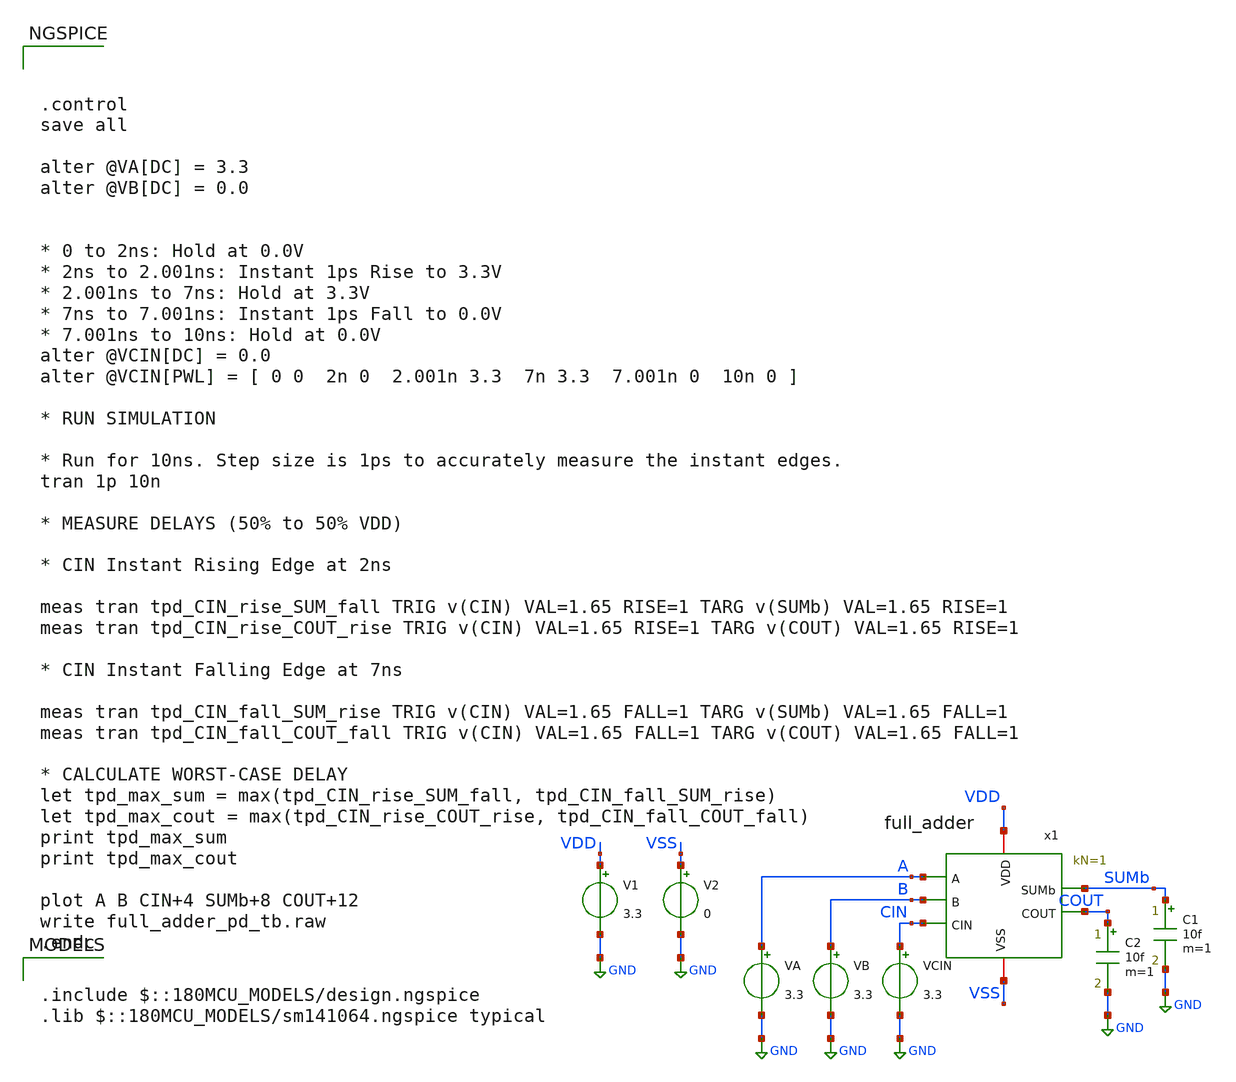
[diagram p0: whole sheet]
** sch_path: CAD4/full_adder_pd_tb.sch
**.subckt full_adder_pd_tb
V1 VDD GND 3.3
VA A GND 3.3
VB B GND 3.3
VCIN CIN GND 3.3
C1 SUMb GND 10f m=1
V2 VSS GND 0
x1 VDD VSS A B CIN SUMb COUT full_adder kN=1 kM=1
C2 COUT GND 10f m=1
**** begin user architecture code

.include $::180MCU_MODELS/design.ngspice
.lib $::180MCU_MODELS/sm141064.ngspice typical




.control
save all

alter @VA[DC] = 3.3
alter @VB[DC] = 0.0


* 0 to 2ns: Hold at 0.0V
* 2ns to 2.001ns: Instant 1ps Rise to 3.3V
* 2.001ns to 7ns: Hold at 3.3V
* 7ns to 7.001ns: Instant 1ps Fall to 0.0V
* 7.001ns to 10ns: Hold at 0.0V
alter @VCIN[DC] = 0.0
alter @VCIN[PWL] = [ 0 0  2n 0  2.001n 3.3  7n 3.3  7.001n 0  10n 0 ]

* RUN SIMULATION

* Run for 10ns. Step size is 1ps to accurately measure the instant edges.
tran 1p 10n

* MEASURE DELAYS (50% to 50% VDD)

* CIN Instant Rising Edge at 2ns

meas tran tpd_CIN_rise_SUM_fall TRIG v(CIN) VAL=1.65 RISE=1 TARG v(SUMb) VAL=1.65 RISE=1
meas tran tpd_CIN_rise_COUT_rise TRIG v(CIN) VAL=1.65 RISE=1 TARG v(COUT) VAL=1.65 RISE=1

* CIN Instant Falling Edge at 7ns

meas tran tpd_CIN_fall_SUM_rise TRIG v(CIN) VAL=1.65 FALL=1 TARG v(SUMb) VAL=1.65 FALL=1
meas tran tpd_CIN_fall_COUT_fall TRIG v(CIN) VAL=1.65 FALL=1 TARG v(COUT) VAL=1.65 FALL=1

* CALCULATE WORST-CASE DELAY
let tpd_max_sum = max(tpd_CIN_rise_SUM_fall, tpd_CIN_fall_SUM_rise)
let tpd_max_cout = max(tpd_CIN_rise_COUT_rise, tpd_CIN_fall_COUT_fall)
print tpd_max_sum
print tpd_max_cout

plot A B CIN+4 SUMb+8 COUT+12
write full_adder_pd_tb.raw
.endc


**** end user architecture code
**.ends

* expanding   symbol:  engn1600-team1/CAD4/full_adder.sym # of pins=7
** sym_path: CAD4/full_adder.sym
** sch_path: CAD4/full_adder.sch
.subckt full_adder VDD VSS A B CIN SUMb COUT  kN=1 kM=1
*.iopin VDD
*.iopin VSS
*.ipin A
*.ipin B
*.ipin CIN
*.opin SUMb
*.opin COUT
XM1 net1 B VDD VDD pfet_03v3 L=0.28u W=0.72u nf=1 ad='int((nf+1)/2) * W/nf * 0.18u' as='int((nf+2)/2) * W/nf * 0.18u'
+ pd='2*int((nf+1)/2) * (W/nf + 0.18u)' ps='2*int((nf+2)/2) * (W/nf + 0.18u)' nrd='0.18u / W' nrs='0.18u / W'
+ sa=0 sb=0 sd=0 m=1
XM2 net4 A net1 VDD pfet_03v3 L=0.28u W=0.72u nf=1 ad='int((nf+1)/2) * W/nf * 0.18u' as='int((nf+2)/2) * W/nf * 0.18u'
+ pd='2*int((nf+1)/2) * (W/nf + 0.18u)' ps='2*int((nf+2)/2) * (W/nf + 0.18u)' nrd='0.18u / W' nrs='0.18u / W'
+ sa=0 sb=0 sd=0 m=1
XM3 net3 A VDD VDD pfet_03v3 L=0.28u W=0.72u nf=1 ad='int((nf+1)/2) * W/nf * 0.18u' as='int((nf+2)/2) * W/nf * 0.18u'
+ pd='2*int((nf+1)/2) * (W/nf + 0.18u)' ps='2*int((nf+2)/2) * (W/nf + 0.18u)' nrd='0.18u / W' nrs='0.18u / W'
+ sa=0 sb=0 sd=0 m=1
XM4 net3 B VDD VDD pfet_03v3 L=0.28u W=0.72u nf=1 ad='int((nf+1)/2) * W/nf * 0.18u' as='int((nf+2)/2) * W/nf * 0.18u'
+ pd='2*int((nf+1)/2) * (W/nf + 0.18u)' ps='2*int((nf+2)/2) * (W/nf + 0.18u)' nrd='0.18u / W' nrs='0.18u / W'
+ sa=0 sb=0 sd=0 m=1
XM5 net4 CIN net3 VDD pfet_03v3 L=0.28u W=0.72u nf=1 ad='int((nf+1)/2) * W/nf * 0.18u' as='int((nf+2)/2) * W/nf * 0.18u'
+ pd='2*int((nf+1)/2) * (W/nf + 0.18u)' ps='2*int((nf+2)/2) * (W/nf + 0.18u)' nrd='0.18u / W' nrs='0.18u / W'
+ sa=0 sb=0 sd=0 m=1
XM6 net4 CIN net5 VSS nfet_03v3 L=0.28u W=0.36u nf=1 ad='int((nf+1)/2) * W/nf * 0.18u' as='int((nf+2)/2) * W/nf * 0.18u'
+ pd='2*int((nf+1)/2) * (W/nf + 0.18u)' ps='2*int((nf+2)/2) * (W/nf + 0.18u)' nrd='0.18u / W' nrs='0.18u / W'
+ sa=0 sb=0 sd=0 m=1
XM7 net2 B VSS VSS nfet_03v3 L=0.28u W=0.36u nf=1 ad='int((nf+1)/2) * W/nf * 0.18u' as='int((nf+2)/2) * W/nf * 0.18u'
+ pd='2*int((nf+1)/2) * (W/nf + 0.18u)' ps='2*int((nf+2)/2) * (W/nf + 0.18u)' nrd='0.18u / W' nrs='0.18u / W'
+ sa=0 sb=0 sd=0 m=1
XM8 net4 A net2 VSS nfet_03v3 L=0.28u W=0.36u nf=1 ad='int((nf+1)/2) * W/nf * 0.18u' as='int((nf+2)/2) * W/nf * 0.18u'
+ pd='2*int((nf+1)/2) * (W/nf + 0.18u)' ps='2*int((nf+2)/2) * (W/nf + 0.18u)' nrd='0.18u / W' nrs='0.18u / W'
+ sa=0 sb=0 sd=0 m=1
XM9 net5 A VSS VSS nfet_03v3 L=0.28u W=0.36u nf=1 ad='int((nf+1)/2) * W/nf * 0.18u' as='int((nf+2)/2) * W/nf * 0.18u'
+ pd='2*int((nf+1)/2) * (W/nf + 0.18u)' ps='2*int((nf+2)/2) * (W/nf + 0.18u)' nrd='0.18u / W' nrs='0.18u / W'
+ sa=0 sb=0 sd=0 m=1
XM10 net5 B VSS VSS nfet_03v3 L=0.28u W=0.36u nf=1 ad='int((nf+1)/2) * W/nf * 0.18u' as='int((nf+2)/2) * W/nf * 0.18u'
+ pd='2*int((nf+1)/2) * (W/nf + 0.18u)' ps='2*int((nf+2)/2) * (W/nf + 0.18u)' nrd='0.18u / W' nrs='0.18u / W'
+ sa=0 sb=0 sd=0 m=1
XM11 SUMb net4 net7 VDD pfet_03v3 L=0.28u W='kN*0.72u' nf=1 ad='int((nf+1)/2) * W/nf * 0.18u' as='int((nf+2)/2) * W/nf * 0.18u'
+ pd='2*int((nf+1)/2) * (W/nf + 0.18u)' ps='2*int((nf+2)/2) * (W/nf + 0.18u)' nrd='0.18u / W' nrs='0.18u / W'
+ sa=0 sb=0 sd=0 m=1
XM12 net7 A VDD VDD pfet_03v3 L=0.28u W=0.72u nf=1 ad='int((nf+1)/2) * W/nf * 0.18u' as='int((nf+2)/2) * W/nf * 0.18u'
+ pd='2*int((nf+1)/2) * (W/nf + 0.18u)' ps='2*int((nf+2)/2) * (W/nf + 0.18u)' nrd='0.18u / W' nrs='0.18u / W'
+ sa=0 sb=0 sd=0 m=1
XM13 net7 CIN VDD VDD pfet_03v3 L=0.28u W=0.72u nf=1 ad='int((nf+1)/2) * W/nf * 0.18u' as='int((nf+2)/2) * W/nf * 0.18u'
+ pd='2*int((nf+1)/2) * (W/nf + 0.18u)' ps='2*int((nf+2)/2) * (W/nf + 0.18u)' nrd='0.18u / W' nrs='0.18u / W'
+ sa=0 sb=0 sd=0 m=1
XM14 net7 B VDD VDD pfet_03v3 L=0.28u W=0.72u nf=1 ad='int((nf+1)/2) * W/nf * 0.18u' as='int((nf+2)/2) * W/nf * 0.18u'
+ pd='2*int((nf+1)/2) * (W/nf + 0.18u)' ps='2*int((nf+2)/2) * (W/nf + 0.18u)' nrd='0.18u / W' nrs='0.18u / W'
+ sa=0 sb=0 sd=0 m=1
XM15 net8 A net9 VDD pfet_03v3 L=0.28u W=0.72u nf=1 ad='int((nf+1)/2) * W/nf * 0.18u' as='int((nf+2)/2) * W/nf * 0.18u'
+ pd='2*int((nf+1)/2) * (W/nf + 0.18u)' ps='2*int((nf+2)/2) * (W/nf + 0.18u)' nrd='0.18u / W' nrs='0.18u / W'
+ sa=0 sb=0 sd=0 m=1
XM16 SUMb CIN net8 VDD pfet_03v3 L=0.28u W=0.72u nf=1 ad='int((nf+1)/2) * W/nf * 0.18u' as='int((nf+2)/2) * W/nf * 0.18u'
+ pd='2*int((nf+1)/2) * (W/nf + 0.18u)' ps='2*int((nf+2)/2) * (W/nf + 0.18u)' nrd='0.18u / W' nrs='0.18u / W'
+ sa=0 sb=0 sd=0 m=1
XM17 net9 B VDD VDD pfet_03v3 L=0.28u W=0.72u nf=1 ad='int((nf+1)/2) * W/nf * 0.18u' as='int((nf+2)/2) * W/nf * 0.18u'
+ pd='2*int((nf+1)/2) * (W/nf + 0.18u)' ps='2*int((nf+2)/2) * (W/nf + 0.18u)' nrd='0.18u / W' nrs='0.18u / W'
+ sa=0 sb=0 sd=0 m=1
XM18 SUMb net4 net6 VSS nfet_03v3 L=0.28u W=0.36u nf=1 ad='int((nf+1)/2) * W/nf * 0.18u' as='int((nf+2)/2) * W/nf * 0.18u'
+ pd='2*int((nf+1)/2) * (W/nf + 0.18u)' ps='2*int((nf+2)/2) * (W/nf + 0.18u)' nrd='0.18u / W' nrs='0.18u / W'
+ sa=0 sb=0 sd=0 m=1
XM19 net6 B VSS VSS nfet_03v3 L=0.28u W=0.36u nf=1 ad='int((nf+1)/2) * W/nf * 0.18u' as='int((nf+2)/2) * W/nf * 0.18u'
+ pd='2*int((nf+1)/2) * (W/nf + 0.18u)' ps='2*int((nf+2)/2) * (W/nf + 0.18u)' nrd='0.18u / W' nrs='0.18u / W'
+ sa=0 sb=0 sd=0 m=1
XM20 net6 A VSS VSS nfet_03v3 L=0.28u W=0.36u nf=1 ad='int((nf+1)/2) * W/nf * 0.18u' as='int((nf+2)/2) * W/nf * 0.18u'
+ pd='2*int((nf+1)/2) * (W/nf + 0.18u)' ps='2*int((nf+2)/2) * (W/nf + 0.18u)' nrd='0.18u / W' nrs='0.18u / W'
+ sa=0 sb=0 sd=0 m=1
XM21 net6 CIN VSS VSS nfet_03v3 L=0.28u W=0.36u nf=1 ad='int((nf+1)/2) * W/nf * 0.18u' as='int((nf+2)/2) * W/nf * 0.18u'
+ pd='2*int((nf+1)/2) * (W/nf + 0.18u)' ps='2*int((nf+2)/2) * (W/nf + 0.18u)' nrd='0.18u / W' nrs='0.18u / W'
+ sa=0 sb=0 sd=0 m=1
XM22 SUMb CIN net11 VSS nfet_03v3 L=0.28u W=0.36u nf=1 ad='int((nf+1)/2) * W/nf * 0.18u' as='int((nf+2)/2) * W/nf * 0.18u'
+ pd='2*int((nf+1)/2) * (W/nf + 0.18u)' ps='2*int((nf+2)/2) * (W/nf + 0.18u)' nrd='0.18u / W' nrs='0.18u / W'
+ sa=0 sb=0 sd=0 m=1
XM23 net11 A net10 VSS nfet_03v3 L=0.28u W=0.36u nf=1 ad='int((nf+1)/2) * W/nf * 0.18u' as='int((nf+2)/2) * W/nf * 0.18u'
+ pd='2*int((nf+1)/2) * (W/nf + 0.18u)' ps='2*int((nf+2)/2) * (W/nf + 0.18u)' nrd='0.18u / W' nrs='0.18u / W'
+ sa=0 sb=0 sd=0 m=1
XM24 net10 B VSS VSS nfet_03v3 L=0.28u W=0.36u nf=1 ad='int((nf+1)/2) * W/nf * 0.18u' as='int((nf+2)/2) * W/nf * 0.18u'
+ pd='2*int((nf+1)/2) * (W/nf + 0.18u)' ps='2*int((nf+2)/2) * (W/nf + 0.18u)' nrd='0.18u / W' nrs='0.18u / W'
+ sa=0 sb=0 sd=0 m=1
XM25 COUT net4 VDD VDD pfet_03v3 L=0.28u W=1.44u nf=1 ad='int((nf+1)/2) * W/nf * 0.18u' as='int((nf+2)/2) * W/nf * 0.18u'
+ pd='2*int((nf+1)/2) * (W/nf + 0.18u)' ps='2*int((nf+2)/2) * (W/nf + 0.18u)' nrd='0.18u / W' nrs='0.18u / W'
+ sa=0 sb=0 sd=0 m=1
XM26 COUT net4 VSS VSS nfet_03v3 L=0.28u W=0.72u nf=1 ad='int((nf+1)/2) * W/nf * 0.18u' as='int((nf+2)/2) * W/nf * 0.18u'
+ pd='2*int((nf+1)/2) * (W/nf + 0.18u)' ps='2*int((nf+2)/2) * (W/nf + 0.18u)' nrd='0.18u / W' nrs='0.18u / W'
+ sa=0 sb=0 sd=0 m=1
**** begin user architecture code


.param kN=1


**** end user architecture code
.ends

.GLOBAL GND
.end
